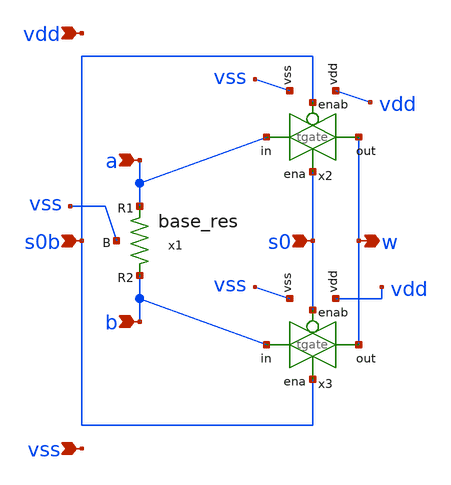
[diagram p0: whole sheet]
** sch_path: xschem/1b_pot.sch
**.subckt 1b_pot s0 s0b vdd vss a b w
*.ipin s0
*.ipin s0b
*.ipin vdd
*.ipin vss
*.ipin a
*.ipin b
*.opin w
x1 a b vss base_res
x2 vdd s0b a w s0 vss tgate
x3 vdd s0 b w s0b vss tgate
**.ends

* expanding   symbol:  xschem/base_res.sym # of pins=3
** sym_path: xschem/base_res.sym
** sch_path: xschem/base_res.sch
.subckt base_res R1 R2 B
*.iopin R1
*.iopin R2
*.iopin B
XR2 R2 R1 B sky130_fd_pr__res_high_po_2p85 L=0.57 mult=1 m=1
.ends


* expanding   symbol:  xschem/tgate.sym # of pins=6
** sym_path: xschem/tgate.sym
** sch_path: xschem/tgate.sch
.subckt tgate vdd enab in out ena vss
*.ipin enab
*.ipin ena
*.ipin in
*.opin out
*.iopin vdd
*.iopin vss
XMn out ena in vss sky130_fd_pr__nfet_g5v0d10v5 L=0.5 W=80 nf=4 ad='int((nf+1)/2) * W/nf * 0.29' as='int((nf+2)/2) * W/nf * 0.29'
+ pd='2*int((nf+1)/2) * (W/nf + 0.29)' ps='2*int((nf+2)/2) * (W/nf + 0.29)' nrd='0.29 / W' nrs='0.29 / W'
+ sa=0 sb=0 sd=0 mult=1 m=1
XMp out enab in vdd sky130_fd_pr__pfet_g5v0d10v5 L=0.5 W=80 nf=4 ad='int((nf+1)/2) * W/nf * 0.29' as='int((nf+2)/2) * W/nf * 0.29'
+ pd='2*int((nf+1)/2) * (W/nf + 0.29)' ps='2*int((nf+2)/2) * (W/nf + 0.29)' nrd='0.29 / W' nrs='0.29 / W'
+ sa=0 sb=0 sd=0 mult=1 m=1
.ends

.end
